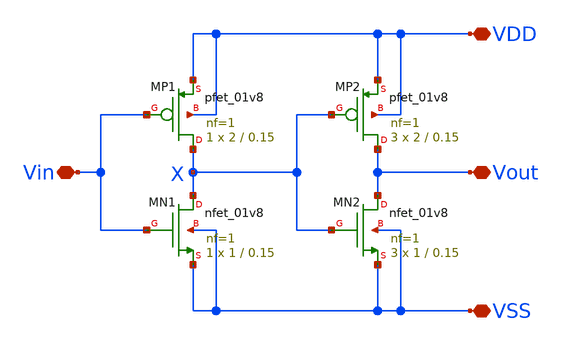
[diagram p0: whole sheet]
** sch_path: xschem/rvco_11st_buffer.sch
**.subckt rvco_11st_buffer VDD Vin Vout VSS
*.iopin VDD
*.iopin Vin
*.iopin Vout
*.iopin VSS
XMP1 X Vin VDD VDD sky130_fd_pr__pfet_01v8 L=0.15 W=2 nf=1 ad='int((nf+1)/2) * W/nf * 0.29' as='int((nf+2)/2) * W/nf * 0.29'
+ pd='2*int((nf+1)/2) * (W/nf + 0.29)' ps='2*int((nf+2)/2) * (W/nf + 0.29)' nrd='0.29 / W' nrs='0.29 / W'
+ sa=0 sb=0 sd=0 mult=1 m=1
XMP2 Vout X VDD VDD sky130_fd_pr__pfet_01v8 L=0.15 W=2 nf=1 ad='int((nf+1)/2) * W/nf * 0.29' as='int((nf+2)/2) * W/nf * 0.29'
+ pd='2*int((nf+1)/2) * (W/nf + 0.29)' ps='2*int((nf+2)/2) * (W/nf + 0.29)' nrd='0.29 / W' nrs='0.29 / W'
+ sa=0 sb=0 sd=0 mult=3 m=3
XMN1 X Vin VSS VSS sky130_fd_pr__nfet_01v8 L=0.15 W=1 nf=1 ad='int((1 + 1)/2) * 1 / 1 * 0.29' as='int((1 + 2)/2) * 1 / 1 * 0.29'
+ pd='2*int((1 + 1)/2) * (1 / 1 + 0.29)' ps='2*int((1 + 2)/2) * (1 / 1 + 0.29)' nrd='0.29 / 1 ' nrs='0.29 / 1 '
+ sa=0 sb=0 sd=0 mult=1 m=1
XMN2 Vout X VSS VSS sky130_fd_pr__nfet_01v8 L=0.15 W=1 nf=1 ad='int((1 + 1)/2) * 1 / 1 * 0.29' as='int((1 + 2)/2) * 1 / 1 * 0.29'
+ pd='2*int((1 + 1)/2) * (1 / 1 + 0.29)' ps='2*int((1 + 2)/2) * (1 / 1 + 0.29)' nrd='0.29 / 1 ' nrs='0.29 / 1 '
+ sa=0 sb=0 sd=0 mult=3 m=3
**.ends
.end
